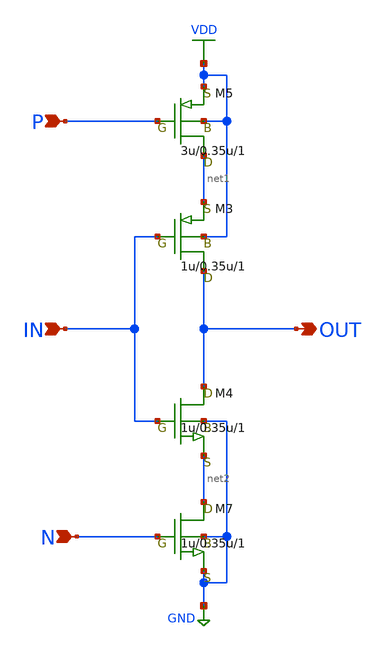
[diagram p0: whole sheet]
** sch_path: LR_hokari/LR_Work2/symbol/CLOCKEDINVERTER.sch
**.subckt CLOCKEDINVERTER OUT IN P N
*.opin OUT
*.ipin IN
*.ipin P
*.ipin N
M3 OUT IN net1 VDD pch w=1u l=0.35u as=0 ps=0 ad=0 pd=0 m=1
M4 OUT IN net2 GND nch w=1u l=0.35u as=0 ps=0 ad=0 pd=0 m=1
M5 net1 P VDD VDD pch w=3u l=0.35u as=0 ps=0 ad=0 pd=0 m=1
M7 net2 N GND GND nch w=1u l=0.35u as=0 ps=0 ad=0 pd=0 m=1
**.ends
.GLOBAL VDD
.GLOBAL GND
.end
